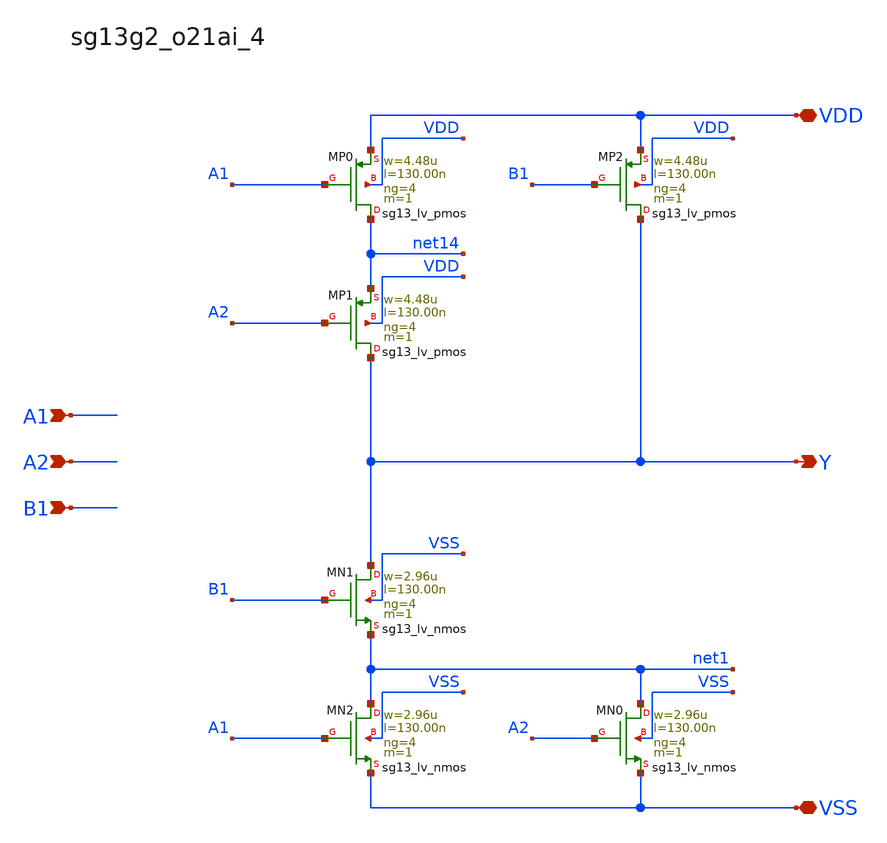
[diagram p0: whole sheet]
** sch_path: outputs/sg13g2_cells/cells/sg13g2_o21ai_4/sg13g2_o21ai_4.sch
**.subckt sg13g2_o21ai_4 Y A1 A2 B1 VDD VSS
*.opin Y
*.ipin A1
*.ipin A2
*.ipin B1
*.iopin VDD
*.iopin VSS
XMP0 net14 A1 VDD VDD sg13_lv_pmos w=4.48u l=130.00n ng=4 m=1 mm_ok=1
XMP1 Y A2 net14 VDD sg13_lv_pmos w=4.48u l=130.00n ng=4 m=1 mm_ok=1
XMP2 Y B1 VDD VDD sg13_lv_pmos w=4.48u l=130.00n ng=4 m=1 mm_ok=1
XMN0 net1 A2 VSS VSS sg13_lv_nmos w=2.96u l=130.00n ng=4 m=1 mm_ok=1
XMN2 net1 A1 VSS VSS sg13_lv_nmos w=2.96u l=130.00n ng=4 m=1 mm_ok=1
XMN1 Y B1 net1 VSS sg13_lv_nmos w=2.96u l=130.00n ng=4 m=1 mm_ok=1
**.ends
.end
